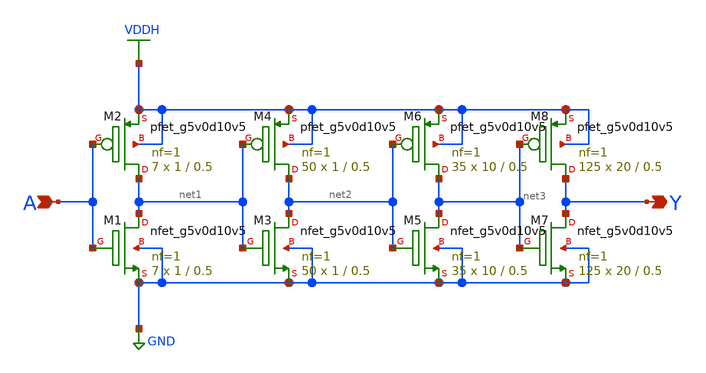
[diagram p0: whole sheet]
** sch_path: Ene_Thompson/drive_train.sch
**.subckt drive_train Y A
*.opin Y
*.ipin A
XM1 net1 A GND GND sky130_fd_pr__nfet_g5v0d10v5 L=0.5 W=1 nf=1 ad='int((nf+1)/2) * W/nf * 0.29' as='int((nf+2)/2) * W/nf * 0.29'
+ pd='2*int((nf+1)/2) * (W/nf + 0.29)' ps='2*int((nf+2)/2) * (W/nf + 0.29)' nrd='0.29 / W' nrs='0.29 / W'
+ sa=0 sb=0 sd=0 mult=7 m=7
XM2 net1 A VDDH VDDH sky130_fd_pr__pfet_g5v0d10v5 L=0.5 W=1 nf=1 ad='int((nf+1)/2) * W/nf * 0.29' as='int((nf+2)/2) * W/nf * 0.29'
+ pd='2*int((nf+1)/2) * (W/nf + 0.29)' ps='2*int((nf+2)/2) * (W/nf + 0.29)' nrd='0.29 / W' nrs='0.29 / W'
+ sa=0 sb=0 sd=0 mult=7 m=7
XM3 net2 net1 GND GND sky130_fd_pr__nfet_g5v0d10v5 L=0.5 W=1 nf=1 ad='int((nf+1)/2) * W/nf * 0.29' as='int((nf+2)/2) * W/nf * 0.29'
+ pd='2*int((nf+1)/2) * (W/nf + 0.29)' ps='2*int((nf+2)/2) * (W/nf + 0.29)' nrd='0.29 / W' nrs='0.29 / W'
+ sa=0 sb=0 sd=0 mult=50 m=50
XM4 net2 net1 VDDH VDDH sky130_fd_pr__pfet_g5v0d10v5 L=0.5 W=1 nf=1 ad='int((nf+1)/2) * W/nf * 0.29'
+ as='int((nf+2)/2) * W/nf * 0.29' pd='2*int((nf+1)/2) * (W/nf + 0.29)' ps='2*int((nf+2)/2) * (W/nf + 0.29)'
+ nrd='0.29 / W' nrs='0.29 / W' sa=0 sb=0 sd=0 mult=50 m=50
XM5 net3 net2 GND GND sky130_fd_pr__nfet_g5v0d10v5 L=0.5 W=10 nf=1 ad='int((nf+1)/2) * W/nf * 0.29' as='int((nf+2)/2) * W/nf * 0.29'
+ pd='2*int((nf+1)/2) * (W/nf + 0.29)' ps='2*int((nf+2)/2) * (W/nf + 0.29)' nrd='0.29 / W' nrs='0.29 / W'
+ sa=0 sb=0 sd=0 mult=35 m=35
XM6 net3 net2 VDDH VDDH sky130_fd_pr__pfet_g5v0d10v5 L=0.5 W=10 nf=1 ad='int((nf+1)/2) * W/nf * 0.29'
+ as='int((nf+2)/2) * W/nf * 0.29' pd='2*int((nf+1)/2) * (W/nf + 0.29)' ps='2*int((nf+2)/2) * (W/nf + 0.29)'
+ nrd='0.29 / W' nrs='0.29 / W' sa=0 sb=0 sd=0 mult=35 m=35
XM7 Y net3 GND GND sky130_fd_pr__nfet_g5v0d10v5 L=0.5 W=20 nf=1 ad='int((nf+1)/2) * W/nf * 0.29' as='int((nf+2)/2) * W/nf * 0.29'
+ pd='2*int((nf+1)/2) * (W/nf + 0.29)' ps='2*int((nf+2)/2) * (W/nf + 0.29)' nrd='0.29 / W' nrs='0.29 / W'
+ sa=0 sb=0 sd=0 mult=125 m=125
XM8 Y net3 VDDH VDDH sky130_fd_pr__pfet_g5v0d10v5 L=0.5 W=20 nf=1 ad='int((nf+1)/2) * W/nf * 0.29' as='int((nf+2)/2) * W/nf * 0.29'
+ pd='2*int((nf+1)/2) * (W/nf + 0.29)' ps='2*int((nf+2)/2) * (W/nf + 0.29)' nrd='0.29 / W' nrs='0.29 / W'
+ sa=0 sb=0 sd=0 mult=125 m=125
**.ends
.GLOBAL VDDH
.GLOBAL GND
.end
